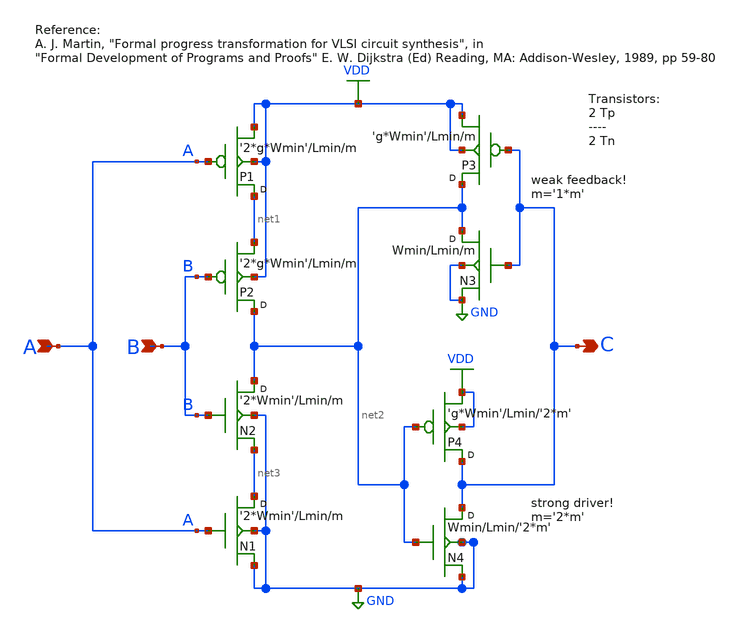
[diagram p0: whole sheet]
** sch_path: Sources/schematics/martin1989.sch
**.subckt martin1989 B C A
*.ipin B
*.opin C
*.ipin A
N2 net2 B net3 GND nmos w='2*Wmin' l=Lmin m=m
P1 net1 A VDD VDD pmos w='2*g*Wmin' l=Lmin m=m
P2 net2 B net1 VDD pmos w='2*g*Wmin' l=Lmin m=m
P4 C net2 VDD VDD pmos w='g*Wmin' l=Lmin m='2*m'
N1 net3 A GND GND nmos w='2*Wmin' l=Lmin m=m
N4 C net2 GND GND nmos w=Wmin l=Lmin m='2*m'
P3 net2 C VDD VDD pmos w='g*Wmin' l=Lmin m=m
N3 net2 C GND GND nmos w=Wmin l=Lmin m=m
**.ends
.GLOBAL GND
.GLOBAL VDD
.end
